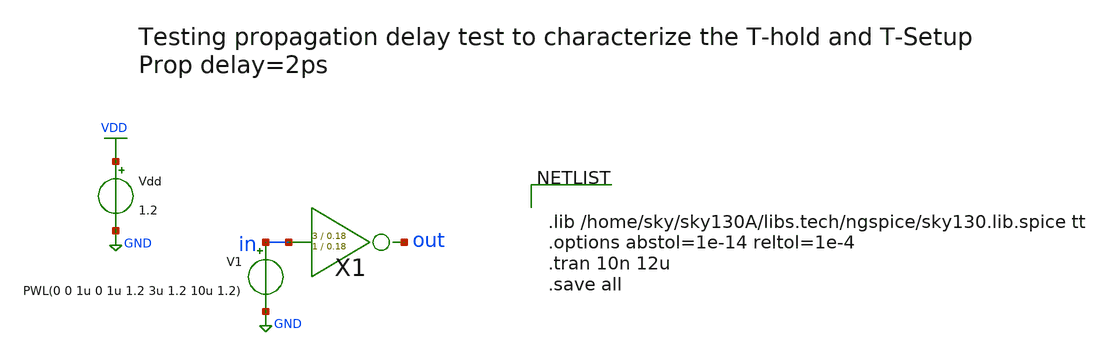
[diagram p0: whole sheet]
** sch_path: xschem/D_flip_flop/inv_prop_delay_tb.sch
**.subckt inv_prop_delay_tb
X1 in out inv Wpmos=3 Lpmos=0.18 Wnmos=1 Lnmos=0.18
V1 in GND PWL(0 0 1u 0 1u 1.2 3u 1.2 10u 1.2)
Vdd VDD GND 1.2
**** begin user architecture code


.lib /home/sky/sky130A/libs.tech/ngspice/sky130.lib.spice tt
.options abstol=1e-14 reltol=1e-4
.tran 10n 12u
.save all


**** end user architecture code
**.ends

* expanding   symbol:  inv/inv.sym # of pins=2
** sym_path: xschem/inv/inv.sym
** sch_path: xschem/inv/inv.sch
.subckt inv in out  Wpmos=3 Lpmos=0.18 Wnmos=1 Lnmos=0.18
*.ipin in
*.iopin out
XM1 out in GND GND sky130_fd_pr__nfet_01v8 L=Lnmos W=Wnmos nf=1 ad='int((nf+1)/2) * W/nf * 0.29' as='int((nf+2)/2) * W/nf * 0.29'
+ pd='2*int((nf+1)/2) * (W/nf + 0.29)' ps='2*int((nf+2)/2) * (W/nf + 0.29)' nrd='0.29 / W' nrs='0.29 / W'
+ sa=0 sb=0 sd=0 mult=1 m=1
XM2 out in VDD VDD sky130_fd_pr__pfet_01v8 L=Lpmos W=Wpmos nf=1 ad='int((nf+1)/2) * W/nf * 0.29' as='int((nf+2)/2) * W/nf * 0.29'
+ pd='2*int((nf+1)/2) * (W/nf + 0.29)' ps='2*int((nf+2)/2) * (W/nf + 0.29)' nrd='0.29 / W' nrs='0.29 / W'
+ sa=0 sb=0 sd=0 mult=1 m=1
.ends

.GLOBAL GND
.GLOBAL VDD
.end
